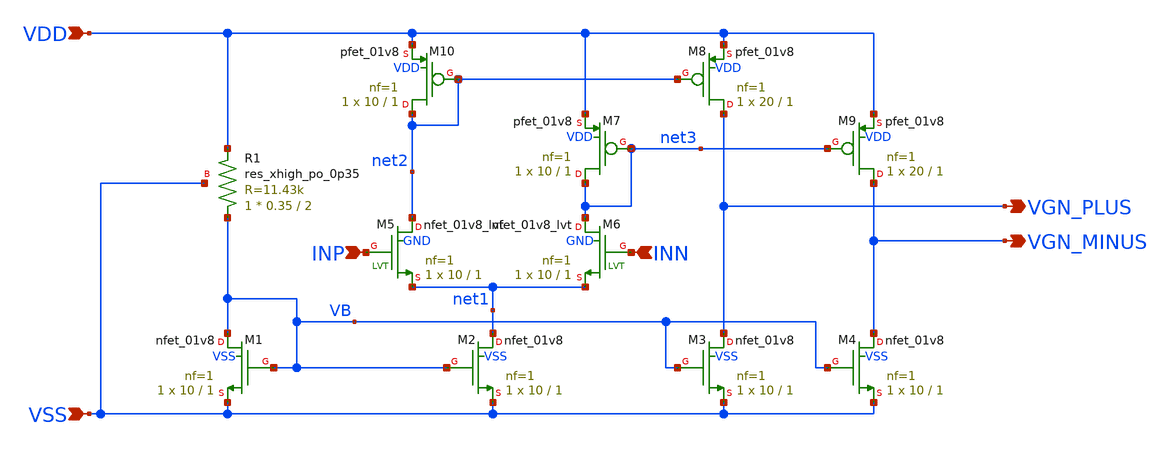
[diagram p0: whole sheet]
** sch_path: preamp.sch
**.subckt preamp VDD VSS INP INN VGN_PLUS VGN_MINUS
*.ipin VDD
*.ipin VSS
*.ipin INP
*.ipin INN
*.opin VGN_PLUS
*.opin VGN_MINUS
XM1 VB VB VSS VSS sky130_fd_pr__nfet_01v8 L=1 W=10 nf=1 ad='int((nf+1)/2) * W/nf * 0.29' as='int((nf+2)/2) * W/nf * 0.29'
+ pd='2*int((nf+1)/2) * (W/nf + 0.29)' ps='2*int((nf+2)/2) * (W/nf + 0.29)' nrd='0.29 / W' nrs='0.29 / W'
+ sa=0 sb=0 sd=0 mult=1 m=1
XM2 net1 VB VSS VSS sky130_fd_pr__nfet_01v8 L=1 W=10 nf=1 ad='int((nf+1)/2) * W/nf * 0.29' as='int((nf+2)/2) * W/nf * 0.29'
+ pd='2*int((nf+1)/2) * (W/nf + 0.29)' ps='2*int((nf+2)/2) * (W/nf + 0.29)' nrd='0.29 / W' nrs='0.29 / W'
+ sa=0 sb=0 sd=0 mult=1 m=1
XM3 VGN_PLUS VB VSS VSS sky130_fd_pr__nfet_01v8 L=1 W=10 nf=1 ad='int((nf+1)/2) * W/nf * 0.29' as='int((nf+2)/2) * W/nf * 0.29'
+ pd='2*int((nf+1)/2) * (W/nf + 0.29)' ps='2*int((nf+2)/2) * (W/nf + 0.29)' nrd='0.29 / W' nrs='0.29 / W'
+ sa=0 sb=0 sd=0 mult=1 m=1
XM4 VGN_MINUS VB VSS VSS sky130_fd_pr__nfet_01v8 L=1 W=10 nf=1 ad='int((nf+1)/2) * W/nf * 0.29' as='int((nf+2)/2) * W/nf * 0.29'
+ pd='2*int((nf+1)/2) * (W/nf + 0.29)' ps='2*int((nf+2)/2) * (W/nf + 0.29)' nrd='0.29 / W' nrs='0.29 / W'
+ sa=0 sb=0 sd=0 mult=1 m=1
XM7 net3 net3 VDD VDD sky130_fd_pr__pfet_01v8 L=1 W=10 nf=1 ad='int((nf+1)/2) * W/nf * 0.29' as='int((nf+2)/2) * W/nf * 0.29'
+ pd='2*int((nf+1)/2) * (W/nf + 0.29)' ps='2*int((nf+2)/2) * (W/nf + 0.29)' nrd='0.29 / W' nrs='0.29 / W'
+ sa=0 sb=0 sd=0 mult=1 m=1
XM8 VGN_PLUS net2 VDD VDD sky130_fd_pr__pfet_01v8 L=1 W=20 nf=1 ad='int((nf+1)/2) * W/nf * 0.29' as='int((nf+2)/2) * W/nf * 0.29'
+ pd='2*int((nf+1)/2) * (W/nf + 0.29)' ps='2*int((nf+2)/2) * (W/nf + 0.29)' nrd='0.29 / W' nrs='0.29 / W'
+ sa=0 sb=0 sd=0 mult=1 m=1
XM9 VGN_MINUS net3 VDD VDD sky130_fd_pr__pfet_01v8 L=1 W=20 nf=1 ad='int((nf+1)/2) * W/nf * 0.29' as='int((nf+2)/2) * W/nf * 0.29'
+ pd='2*int((nf+1)/2) * (W/nf + 0.29)' ps='2*int((nf+2)/2) * (W/nf + 0.29)' nrd='0.29 / W' nrs='0.29 / W'
+ sa=0 sb=0 sd=0 mult=1 m=1
XM10 net2 net2 VDD VDD sky130_fd_pr__pfet_01v8 L=1 W=10 nf=1 ad='int((nf+1)/2) * W/nf * 0.29' as='int((nf+2)/2) * W/nf * 0.29'
+ pd='2*int((nf+1)/2) * (W/nf + 0.29)' ps='2*int((nf+2)/2) * (W/nf + 0.29)' nrd='0.29 / W' nrs='0.29 / W'
+ sa=0 sb=0 sd=0 mult=1 m=1
XR1 VB VDD VSS sky130_fd_pr__res_xhigh_po_0p35 L=2 mult=1 m=1
XM5 net2 INP net1 GND sky130_fd_pr__nfet_01v8_lvt L=1 W=10 nf=1 ad='int((nf+1)/2) * W/nf * 0.29' as='int((nf+2)/2) * W/nf * 0.29'
+ pd='2*int((nf+1)/2) * (W/nf + 0.29)' ps='2*int((nf+2)/2) * (W/nf + 0.29)' nrd='0.29 / W' nrs='0.29 / W'
+ sa=0 sb=0 sd=0 mult=1 m=1
XM6 net3 INN net1 GND sky130_fd_pr__nfet_01v8_lvt L=1 W=10 nf=1 ad='int((nf+1)/2) * W/nf * 0.29' as='int((nf+2)/2) * W/nf * 0.29'
+ pd='2*int((nf+1)/2) * (W/nf + 0.29)' ps='2*int((nf+2)/2) * (W/nf + 0.29)' nrd='0.29 / W' nrs='0.29 / W'
+ sa=0 sb=0 sd=0 mult=1 m=1
**.ends
.end
